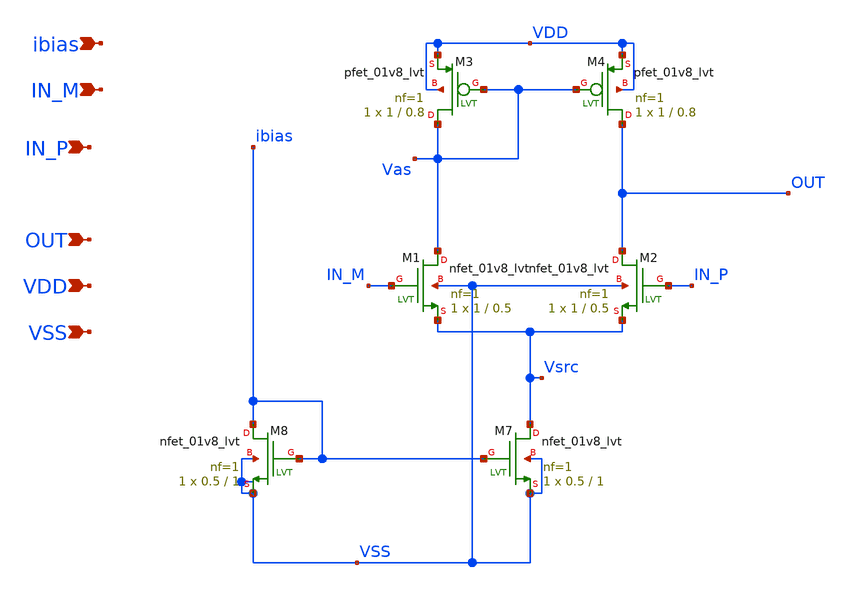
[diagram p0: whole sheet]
** sch_path: OTA1st_lvt_jm.sch
**.subckt OTA1st_lvt_jm IN_M IN_P OUT VDD VSS ibias
*.ipin IN_M
*.ipin IN_P
*.ipin OUT
*.ipin VDD
*.ipin VSS
*.ipin ibias
XM1 Vas IN_M Vsrc VSS sky130_fd_pr__nfet_01v8_lvt L=0.5 W=1 nf=1 ad='int((nf+1)/2) * W/nf * 0.29' as='int((nf+2)/2) * W/nf * 0.29'
+ pd='2*int((nf+1)/2) * (W/nf + 0.29)' ps='2*int((nf+2)/2) * (W/nf + 0.29)' nrd='0.29 / W' nrs='0.29 / W'
+ sa=0 sb=0 sd=0 mult=1 m=1
XM2 OUT IN_P Vsrc VSS sky130_fd_pr__nfet_01v8_lvt L=0.5 W=1 nf=1 ad='int((nf+1)/2) * W/nf * 0.29' as='int((nf+2)/2) * W/nf * 0.29'
+ pd='2*int((nf+1)/2) * (W/nf + 0.29)' ps='2*int((nf+2)/2) * (W/nf + 0.29)' nrd='0.29 / W' nrs='0.29 / W'
+ sa=0 sb=0 sd=0 mult=1 m=1
XM3 Vas Vas VDD VDD sky130_fd_pr__pfet_01v8_lvt L=0.8 W=1 nf=1 ad='int((nf+1)/2) * W/nf * 0.29' as='int((nf+2)/2) * W/nf * 0.29'
+ pd='2*int((nf+1)/2) * (W/nf + 0.29)' ps='2*int((nf+2)/2) * (W/nf + 0.29)' nrd='0.29 / W' nrs='0.29 / W'
+ sa=0 sb=0 sd=0 mult=1 m=1
XM4 OUT Vas VDD VDD sky130_fd_pr__pfet_01v8_lvt L=0.8 W=1 nf=1 ad='int((nf+1)/2) * W/nf * 0.29' as='int((nf+2)/2) * W/nf * 0.29'
+ pd='2*int((nf+1)/2) * (W/nf + 0.29)' ps='2*int((nf+2)/2) * (W/nf + 0.29)' nrd='0.29 / W' nrs='0.29 / W'
+ sa=0 sb=0 sd=0 mult=1 m=1
XM7 Vsrc ibias VSS VSS sky130_fd_pr__nfet_01v8_lvt L=1 W=0.5 nf=1 ad='int((nf+1)/2) * W/nf * 0.29' as='int((nf+2)/2) * W/nf * 0.29'
+ pd='2*int((nf+1)/2) * (W/nf + 0.29)' ps='2*int((nf+2)/2) * (W/nf + 0.29)' nrd='0.29 / W' nrs='0.29 / W'
+ sa=0 sb=0 sd=0 mult=1 m=1
XM8 ibias ibias VSS VSS sky130_fd_pr__nfet_01v8_lvt L=1 W=0.5 nf=1 ad='int((nf+1)/2) * W/nf * 0.29' as='int((nf+2)/2) * W/nf * 0.29'
+ pd='2*int((nf+1)/2) * (W/nf + 0.29)' ps='2*int((nf+2)/2) * (W/nf + 0.29)' nrd='0.29 / W' nrs='0.29 / W'
+ sa=0 sb=0 sd=0 mult=1 m=1
**.ends
.end
